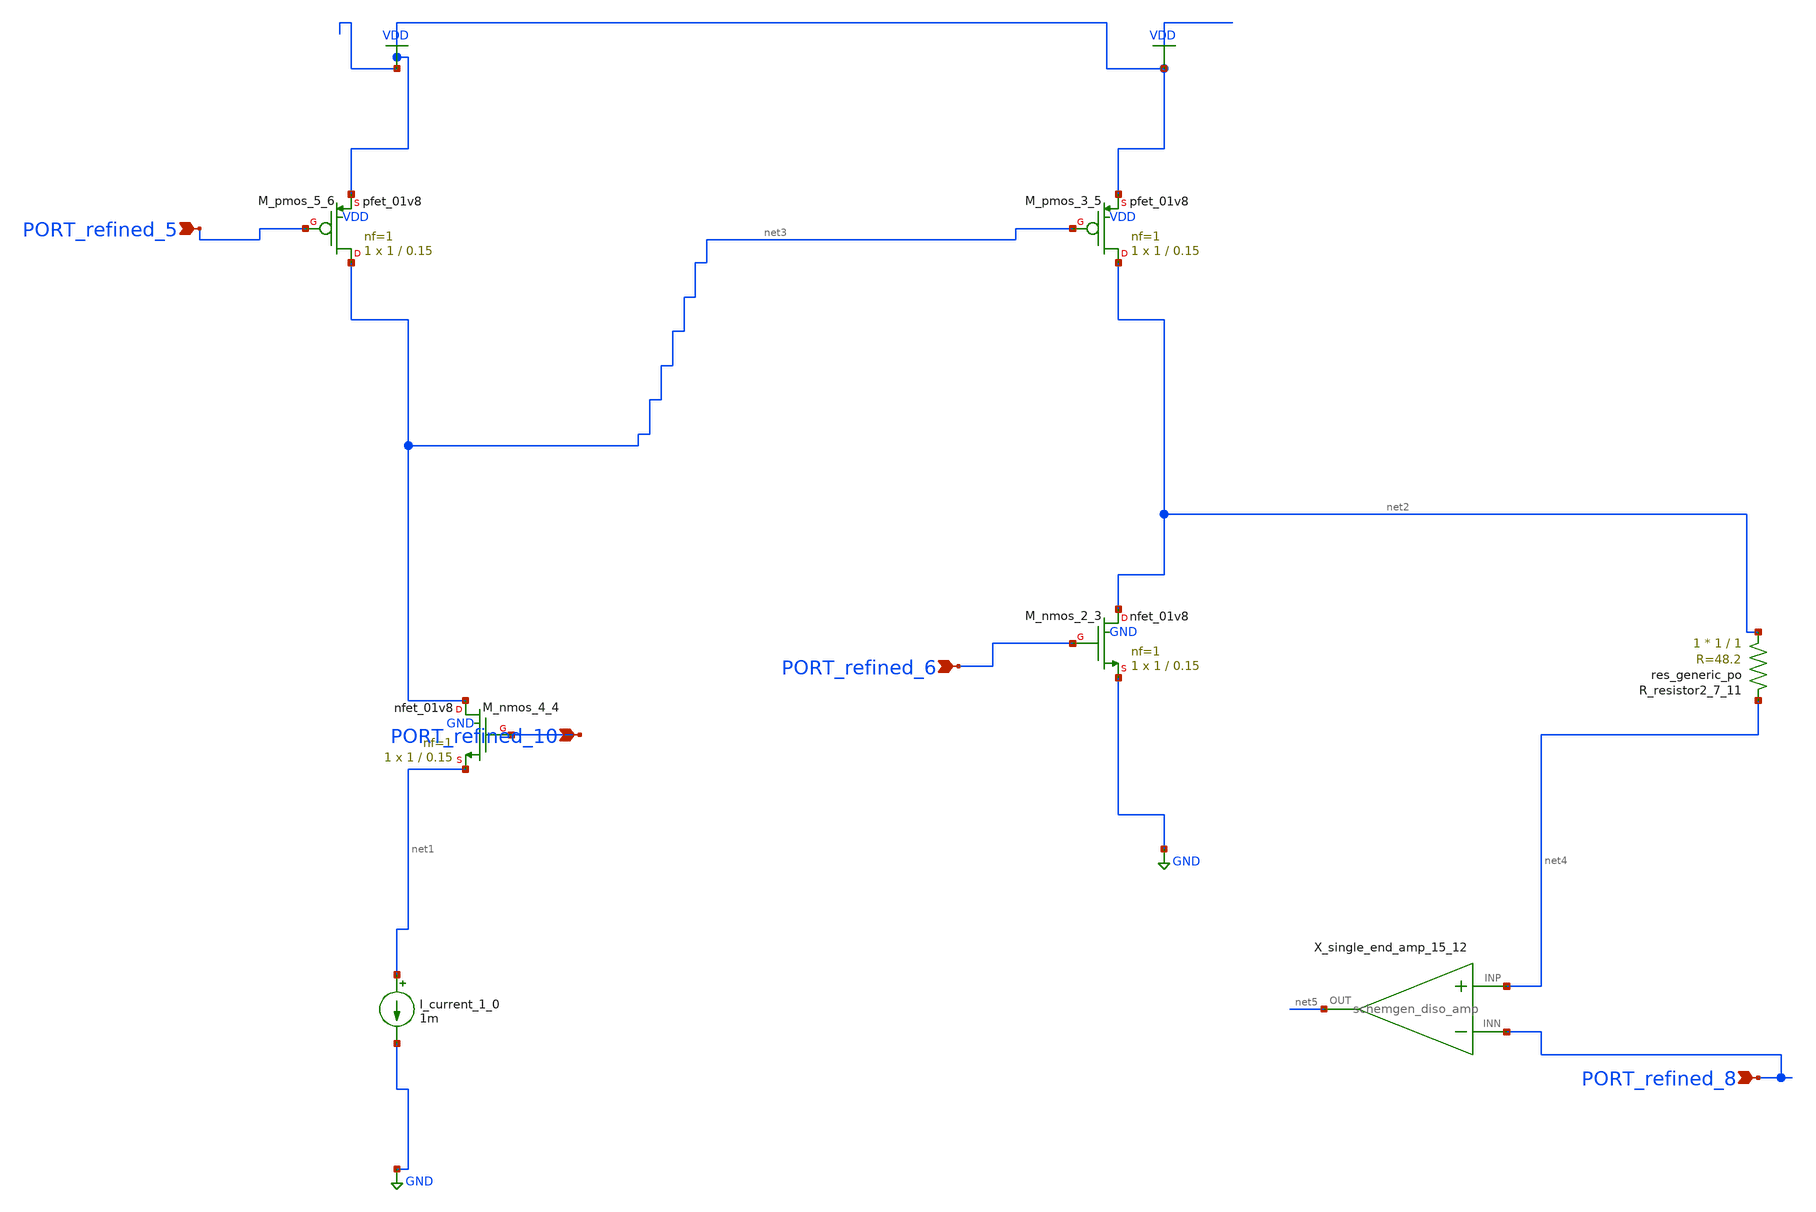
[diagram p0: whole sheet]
** sch_path: schematics/AMSNet/680.sch
**.subckt 680 PORT_refined_6 PORT_refined_5 PORT_refined_8 PORT_refined_10
*.ipin PORT_refined_6
*.ipin PORT_refined_5
*.ipin PORT_refined_8
*.ipin PORT_refined_10
I_current_1_0 net1 GND 1m
XM_nmos_2_3 net2 PORT_refined_6 GND GND sky130_fd_pr__nfet_01v8 L=0.15 W=1 nf=1 ad='int((1 + 1)/2) * 1 / 1 * 0.29'
+ as='int((1 + 2)/2) * 1 / 1 * 0.29' pd='2*int((1 + 1)/2) * (1 / 1 + 0.29)' ps='2*int((1 + 2)/2) * (1 / 1 + 0.29)'
+ nrd='0.29 / 1 ' nrs='0.29 / 1 ' sa=0 sb=0 sd=0 mult=1 m=1
XM_nmos_4_4 net3 PORT_refined_10 net1 GND sky130_fd_pr__nfet_01v8 L=0.15 W=1 nf=1 ad='int((1 + 1)/2) * 1 / 1 * 0.29'
+ as='int((1 + 2)/2) * 1 / 1 * 0.29' pd='2*int((1 + 1)/2) * (1 / 1 + 0.29)' ps='2*int((1 + 2)/2) * (1 / 1 + 0.29)'
+ nrd='0.29 / 1 ' nrs='0.29 / 1 ' sa=0 sb=0 sd=0 mult=1 m=1
XM_pmos_3_5 net2 net3 VDD VDD sky130_fd_pr__pfet_01v8 L=0.15 W=1 nf=1 ad='int((1 + 1)/2) * 1 / 1 * 0.29'
+ as='int((1 + 2)/2) * 1 / 1 * 0.29' pd='2*int((1 + 1)/2) * (1 / 1 + 0.29)' ps='2*int((1 + 2)/2) * (1 / 1 + 0.29)'
+ nrd='0.29 / 1 ' nrs='0.29 / 1 ' sa=0 sb=0 sd=0 mult=1 m=1
XM_pmos_5_6 net3 PORT_refined_5 VDD VDD sky130_fd_pr__pfet_01v8 L=0.15 W=1 nf=1 ad='int((1 + 1)/2) * 1 / 1 * 0.29'
+ as='int((1 + 2)/2) * 1 / 1 * 0.29' pd='2*int((1 + 1)/2) * (1 / 1 + 0.29)' ps='2*int((1 + 2)/2) * (1 / 1 + 0.29)'
+ nrd='0.29 / 1 ' nrs='0.29 / 1 ' sa=0 sb=0 sd=0 mult=1 m=1
XR_resistor2_7_11 net2 net4 sky130_fd_pr__res_generic_po W=1 L=1 m=1
X_single_end_amp_15_12 net4 PORT_refined_8 net5 schemgen_diso_amp
**.ends

* expanding   symbol:  schemgen_diso_amp.sym # of pins=3
** sym_path: symbols/schemgen_diso_amp.sym
.subckt schemgen_diso_amp INP INN OUT
* SchemGen ideal op-amp: Vout = 1e5 * (V(INP) - V(INN))
E1 OUT 0 INP INN 1e5
.ends schemgen_diso_amp
.GLOBAL GND
.GLOBAL VDD
.end
